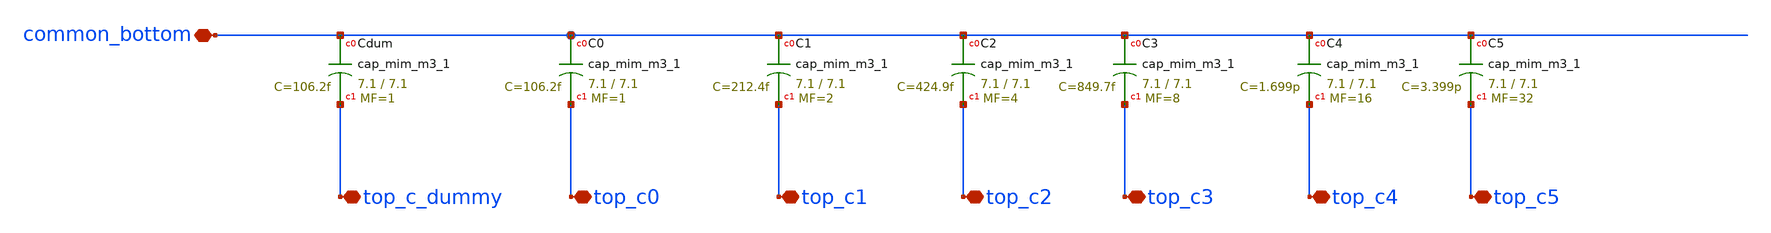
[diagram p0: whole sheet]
** sch_path: SKY130/SAR-ADC/SAR-ADC_1.8V/cap_array_MF.sch
**.subckt cap_array_MF common_bottom top_c1 top_c0 top_c_dummy top_c2 top_c4 top_c5 top_c3
*.iopin common_bottom
*.iopin top_c1
*.iopin top_c0
*.iopin top_c_dummy
*.iopin top_c2
*.iopin top_c4
*.iopin top_c5
*.iopin top_c3
XC0 common_bottom top_c0 sky130_fd_pr__cap_mim_m3_1 W=7.1 L=7.1 MF=1 m=1
XC1 common_bottom top_c1 sky130_fd_pr__cap_mim_m3_1 W=7.1 L=7.1 MF=2 m=2
XC2 common_bottom top_c2 sky130_fd_pr__cap_mim_m3_1 W=7.1 L=7.1 MF=4 m=4
XC3 common_bottom top_c3 sky130_fd_pr__cap_mim_m3_1 W=7.1 L=7.1 MF=8 m=8
XC4 common_bottom top_c4 sky130_fd_pr__cap_mim_m3_1 W=7.1 L=7.1 MF=16 m=16
XC5 common_bottom top_c5 sky130_fd_pr__cap_mim_m3_1 W=7.1 L=7.1 MF=32 m=32
XCdum common_bottom top_c_dummy sky130_fd_pr__cap_mim_m3_1 W=7.1 L=7.1 MF=1 m=1
**.ends
.end
